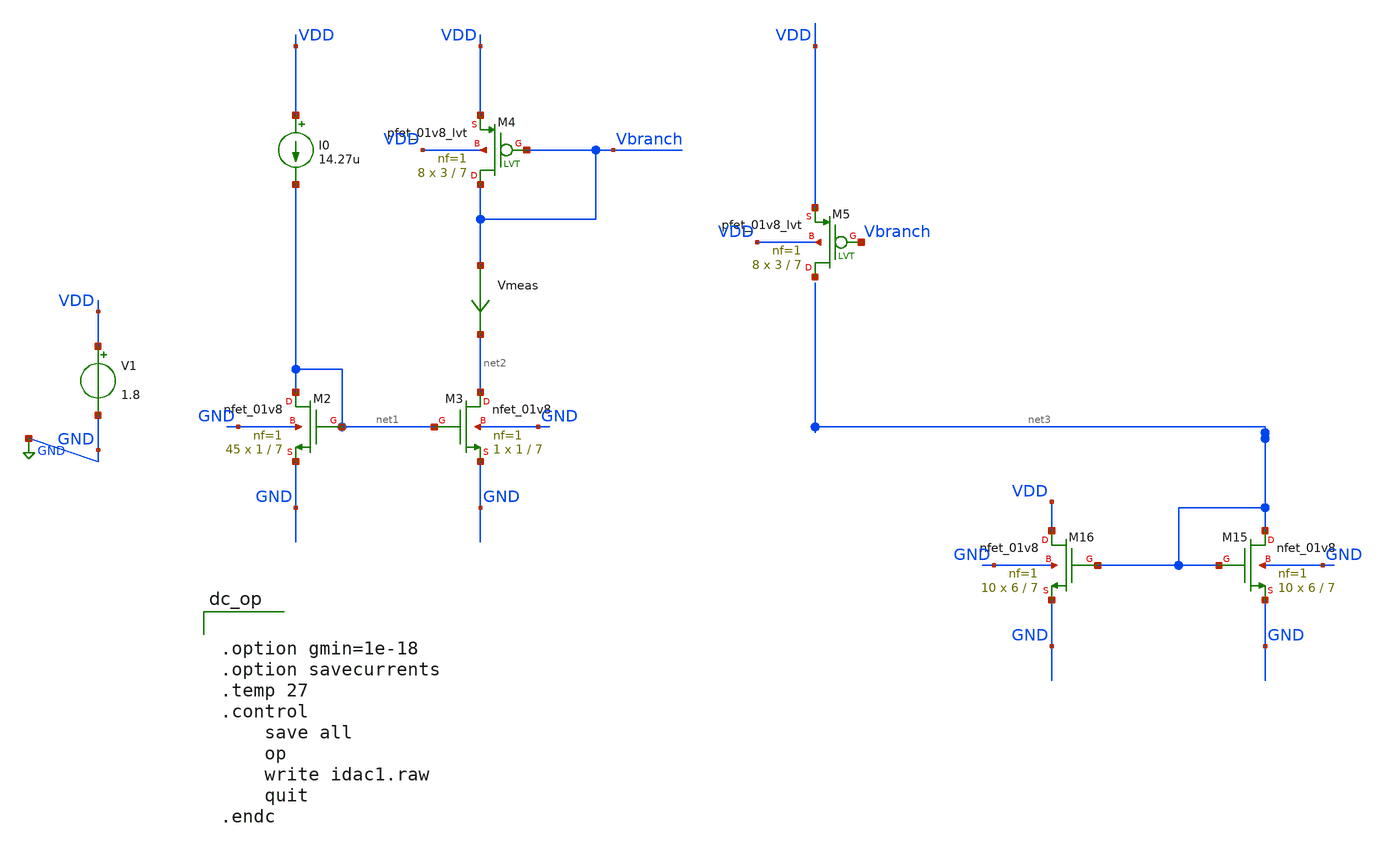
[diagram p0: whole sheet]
** sch_path: xschem/archive/old_blocks/idac1.sch
**.subckt idac1
V1 VDD GND 1.8
XM2 net1 net1 GND GND sky130_fd_pr__nfet_01v8 L=7 W=1 nf=1 ad='int((1 + 1)/2) * 1 / 1 * 0.29' as='int((1 + 2)/2) * 1 / 1 * 0.29'
+ pd='2*int((1 + 1)/2) * (1 / 1 + 0.29)' ps='2*int((1 + 2)/2) * (1 / 1 + 0.29)' nrd='0.29 / 1 ' nrs='0.29 / 1 '
+ sa=0 sb=0 sd=0 mult=45 m=45
XM3 net2 net1 GND GND sky130_fd_pr__nfet_01v8 L=7 W=1 nf=1 ad='int((1 + 1)/2) * 1 / 1 * 0.29' as='int((1 + 2)/2) * 1 / 1 * 0.29'
+ pd='2*int((1 + 1)/2) * (1 / 1 + 0.29)' ps='2*int((1 + 2)/2) * (1 / 1 + 0.29)' nrd='0.29 / 1 ' nrs='0.29 / 1 '
+ sa=0 sb=0 sd=0 mult=1 m=1
XM4 Vbranch Vbranch VDD VDD sky130_fd_pr__pfet_01v8_lvt L=7 W=3 nf=1 ad='int((1 + 1)/2) * 3 / 1 * 0.29'
+ as='int((1 + 2)/2) * 3 / 1 * 0.29' pd='2*int((1 + 1)/2) * (3 / 1 + 0.29)' ps='2*int((1 + 2)/2) * (3 / 1 + 0.29)'
+ nrd='0.29 / 3 ' nrs='0.29 / 3 ' sa=0 sb=0 sd=0 mult=8 m=8
Vmeas Vbranch net2 0
.save i(vmeas)
XM5 net4 Vbranch VDD VDD sky130_fd_pr__pfet_01v8_lvt L=7 W=3 nf=1 ad='int((1 + 1)/2) * 3 / 1 * 0.29'
+ as='int((1 + 2)/2) * 3 / 1 * 0.29' pd='2*int((1 + 1)/2) * (3 / 1 + 0.29)' ps='2*int((1 + 2)/2) * (3 / 1 + 0.29)'
+ nrd='0.29 / 3 ' nrs='0.29 / 3 ' sa=0 sb=0 sd=0 mult=8 m=8
XM15 net3 net3 GND GND sky130_fd_pr__nfet_01v8 L=7 W=6 nf=1 ad='int((1 + 1)/2) * 6 / 1 * 0.29' as='int((1 + 2)/2) * 6 / 1 * 0.29'
+ pd='2*int((1 + 1)/2) * (6 / 1 + 0.29)' ps='2*int((1 + 2)/2) * (6 / 1 + 0.29)' nrd='0.29 / 6 ' nrs='0.29 / 6 '
+ sa=0 sb=0 sd=0 mult=10 m=10
XM16 VDD net3 GND GND sky130_fd_pr__nfet_01v8 L=7 W=6 nf=1 ad='int((1 + 1)/2) * 6 / 1 * 0.29' as='int((1 + 2)/2) * 6 / 1 * 0.29'
+ pd='2*int((1 + 1)/2) * (6 / 1 + 0.29)' ps='2*int((1 + 2)/2) * (6 / 1 + 0.29)' nrd='0.29 / 6 ' nrs='0.29 / 6 '
+ sa=0 sb=0 sd=0 mult=10 m=10
I0 VDD net1 14.27u
**** begin user architecture code


.option gmin=1e-18
.option savecurrents
.temp 27
.control
    save all
    op
    write idac1.raw
    quit
.endc




** opencircuitdesign pdks install
.lib $::SKYWATER_MODELS/sky130.lib.spice tt

**** end user architecture code
**.ends
.GLOBAL GND
.end
